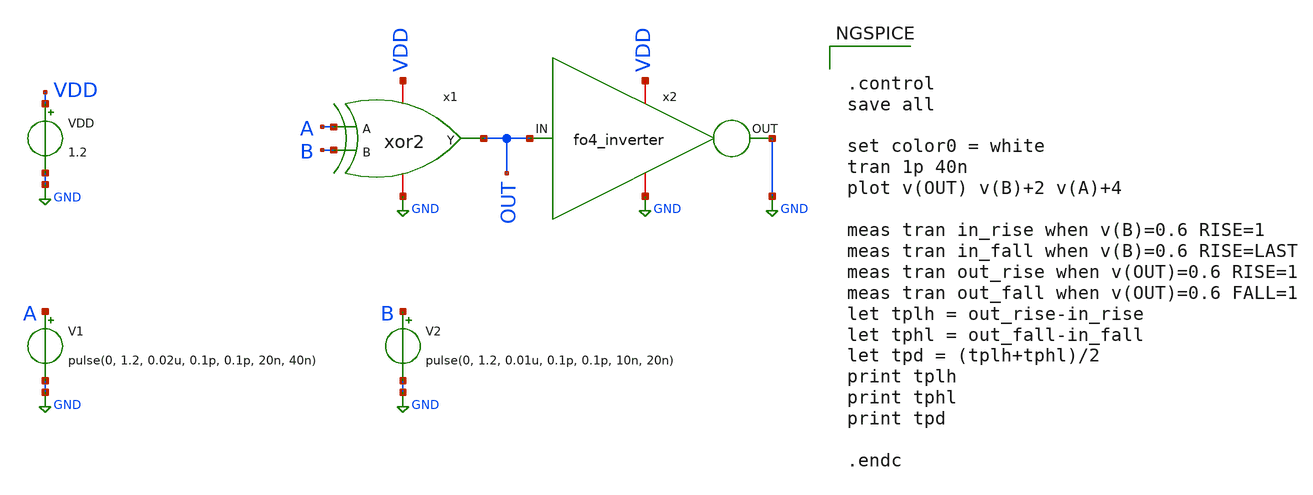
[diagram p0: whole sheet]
** sch_path: design/xor_with_fo4/xor2_tb.sch
**.subckt xor2_tb
x1 OUT A VDD GND B xor2
VDD VDD GND 1.2
V1 A GND pulse(0, 1.2, 0.02u, 0.1p, 0.1p, 20n, 40n)
x2 VDD OUT GND GND fo4_inverter
V2 B GND pulse(0, 1.2, 0.01u, 0.1p, 0.1p, 10n, 20n)
**** begin user architecture code

** opencircuitdesign pdks install
.lib $::SKYWATER_MODELS/sky130.lib.spice tt_mm




.control
save all

set color0 = white
tran 1p 40n
plot v(OUT) v(B)+2 v(A)+4

meas tran in_rise when v(B)=0.6 RISE=1
meas tran in_fall when v(B)=0.6 RISE=LAST
meas tran out_rise when v(OUT)=0.6 RISE=1
meas tran out_fall when v(OUT)=0.6 FALL=1
let tplh = out_rise-in_rise
let tphl = out_fall-in_fall
let tpd = (tplh+tphl)/2
print tplh
print tphl
print tpd

.endc

**** end user architecture code
**.ends

* expanding   symbol:  xor_with_fo4/xor2.sym # of pins=5
** sym_path: design/xor_with_fo4/xor2.sym
** sch_path: design/xor_with_fo4/xor2.sch
.subckt xor2 Y A VDD VSS B
*.opin Y
*.ipin A
*.iopin VDD
*.iopin VSS
*.ipin B
XM11 net1 A VDD VDD sky130_fd_pr__pfet_01v8 L=0.15 W=6 nf=1 ad='int((nf+1)/2) * W/nf * 0.29' as='int((nf+2)/2) * W/nf * 0.29'
+ pd='2*int((nf+1)/2) * (W/nf + 0.29)' ps='2*int((nf+2)/2) * (W/nf + 0.29)' nrd='0.29 / W' nrs='0.29 / W'
+ sa=0 sb=0 sd=0 mult=1 m=1
XM1 net1 B VDD VDD sky130_fd_pr__pfet_01v8 L=0.15 W=6 nf=1 ad='int((nf+1)/2) * W/nf * 0.29' as='int((nf+2)/2) * W/nf * 0.29'
+ pd='2*int((nf+1)/2) * (W/nf + 0.29)' ps='2*int((nf+2)/2) * (W/nf + 0.29)' nrd='0.29 / W' nrs='0.29 / W'
+ sa=0 sb=0 sd=0 mult=1 m=1
XM2 Y inv_B net1 net1 sky130_fd_pr__pfet_01v8 L=0.15 W=6 nf=1 ad='int((nf+1)/2) * W/nf * 0.29' as='int((nf+2)/2) * W/nf * 0.29'
+ pd='2*int((nf+1)/2) * (W/nf + 0.29)' ps='2*int((nf+2)/2) * (W/nf + 0.29)' nrd='0.29 / W' nrs='0.29 / W'
+ sa=0 sb=0 sd=0 mult=1 m=1
XM3 Y inv_A net1 net1 sky130_fd_pr__pfet_01v8 L=0.15 W=6 nf=1 ad='int((nf+1)/2) * W/nf * 0.29' as='int((nf+2)/2) * W/nf * 0.29'
+ pd='2*int((nf+1)/2) * (W/nf + 0.29)' ps='2*int((nf+2)/2) * (W/nf + 0.29)' nrd='0.29 / W' nrs='0.29 / W'
+ sa=0 sb=0 sd=0 mult=1 m=1
XM4 Y A net2 net2 sky130_fd_pr__nfet_01v8 L=0.15 W=1 nf=1 ad='int((1 + 1)/2) * 1 / 1 * 0.29' as='int((1 + 2)/2) * 1 / 1 * 0.29'
+ pd='2*int((1 + 1)/2) * (1 / 1 + 0.29)' ps='2*int((1 + 2)/2) * (1 / 1 + 0.29)' nrd='0.29 / 1 ' nrs='0.29 / 1 '
+ sa=0 sb=0 sd=0 mult=1 m=1
XM5 net2 B VSS VSS sky130_fd_pr__nfet_01v8 L=0.15 W=1 nf=1 ad='int((1 + 1)/2) * 1 / 1 * 0.29' as='int((1 + 2)/2) * 1 / 1 * 0.29'
+ pd='2*int((1 + 1)/2) * (1 / 1 + 0.29)' ps='2*int((1 + 2)/2) * (1 / 1 + 0.29)' nrd='0.29 / 1 ' nrs='0.29 / 1 '
+ sa=0 sb=0 sd=0 mult=1 m=1
XM6 Y inv_A net3 net3 sky130_fd_pr__nfet_01v8 L=0.15 W=1 nf=1 ad='int((1 + 1)/2) * 1 / 1 * 0.29' as='int((1 + 2)/2) * 1 / 1 * 0.29'
+ pd='2*int((1 + 1)/2) * (1 / 1 + 0.29)' ps='2*int((1 + 2)/2) * (1 / 1 + 0.29)' nrd='0.29 / 1 ' nrs='0.29 / 1 '
+ sa=0 sb=0 sd=0 mult=1 m=1
XM7 net3 inv_B VSS VSS sky130_fd_pr__nfet_01v8 L=0.15 W=1 nf=1 ad='int((1 + 1)/2) * 1 / 1 * 0.29' as='int((1 + 2)/2) * 1 / 1 * 0.29'
+ pd='2*int((1 + 1)/2) * (1 / 1 + 0.29)' ps='2*int((1 + 2)/2) * (1 / 1 + 0.29)' nrd='0.29 / 1 ' nrs='0.29 / 1 '
+ sa=0 sb=0 sd=0 mult=1 m=1
XM8 inv_B B VDD VDD sky130_fd_pr__pfet_01v8 L=0.15 W=6 nf=1 ad='int((nf+1)/2) * W/nf * 0.29' as='int((nf+2)/2) * W/nf * 0.29'
+ pd='2*int((nf+1)/2) * (W/nf + 0.29)' ps='2*int((nf+2)/2) * (W/nf + 0.29)' nrd='0.29 / W' nrs='0.29 / W'
+ sa=0 sb=0 sd=0 mult=1 m=1
XM9 inv_B B VSS VSS sky130_fd_pr__nfet_01v8 L=0.15 W=1 nf=1 ad='int((1 + 1)/2) * 1 / 1 * 0.29' as='int((1 + 2)/2) * 1 / 1 * 0.29'
+ pd='2*int((1 + 1)/2) * (1 / 1 + 0.29)' ps='2*int((1 + 2)/2) * (1 / 1 + 0.29)' nrd='0.29 / 1 ' nrs='0.29 / 1 '
+ sa=0 sb=0 sd=0 mult=1 m=1
XM10 inv_A A VDD VDD sky130_fd_pr__pfet_01v8 L=0.15 W=6 nf=1 ad='int((nf+1)/2) * W/nf * 0.29' as='int((nf+2)/2) * W/nf * 0.29'
+ pd='2*int((nf+1)/2) * (W/nf + 0.29)' ps='2*int((nf+2)/2) * (W/nf + 0.29)' nrd='0.29 / W' nrs='0.29 / W'
+ sa=0 sb=0 sd=0 mult=1 m=1
XM12 inv_A A VSS VSS sky130_fd_pr__nfet_01v8 L=0.15 W=1 nf=1 ad='int((1 + 1)/2) * 1 / 1 * 0.29' as='int((1 + 2)/2) * 1 / 1 * 0.29'
+ pd='2*int((1 + 1)/2) * (1 / 1 + 0.29)' ps='2*int((1 + 2)/2) * (1 / 1 + 0.29)' nrd='0.29 / 1 ' nrs='0.29 / 1 '
+ sa=0 sb=0 sd=0 mult=1 m=1
.ends


* expanding   symbol:  inv_with_fo4/fo4_inverter.sym # of pins=4
** sym_path: design/2x1_mux_with_fo4/fo4_inverter.sym
** sch_path: design/2x1_mux_with_fo4/fo4_inverter.sch
.subckt fo4_inverter VDD IN OUT VSS
*.ipin IN
*.iopin VDD
*.iopin VSS
*.opin OUT
x1 VDD OUT IN VSS inverter
x2 VDD OUT IN VSS inverter
x3 VDD OUT IN VSS inverter
x4 VDD OUT IN VSS inverter
.ends


* expanding   symbol:  inverter.sym # of pins=4
** sym_path: design/ALU/inverter.sym
** sch_path: design/ALU/inverter.sch
.subckt inverter VDD OUT IN VSS
*.ipin IN
*.iopin VDD
*.opin OUT
*.iopin VSS
XM2 OUT IN VDD VDD sky130_fd_pr__pfet_01v8 L=0.15 W=0.9 nf=1 ad='int((nf+1)/2) * W/nf * 0.29' as='int((nf+2)/2) * W/nf * 0.29'
+ pd='2*int((nf+1)/2) * (W/nf + 0.29)' ps='2*int((nf+2)/2) * (W/nf + 0.29)' nrd='0.29 / W' nrs='0.29 / W'
+ sa=0 sb=0 sd=0 mult=1 m=1
XM1 OUT IN VSS VSS sky130_fd_pr__nfet_01v8 L=0.15 W=0.42 nf=1 ad='int((1 + 1)/2) * 0.42 / 1 * 0.29' as='int((1 + 2)/2) * 0.42 / 1 * 0.29'
+ pd='2*int((1 + 1)/2) * (0.42 / 1 + 0.29)' ps='2*int((1 + 2)/2) * (0.42 / 1 + 0.29)' nrd='0.29 / 0.42 '
+ nrs='0.29 / 0.42 ' sa=0 sb=0 sd=0 mult=1 m=1
.ends

.GLOBAL GND
.end
